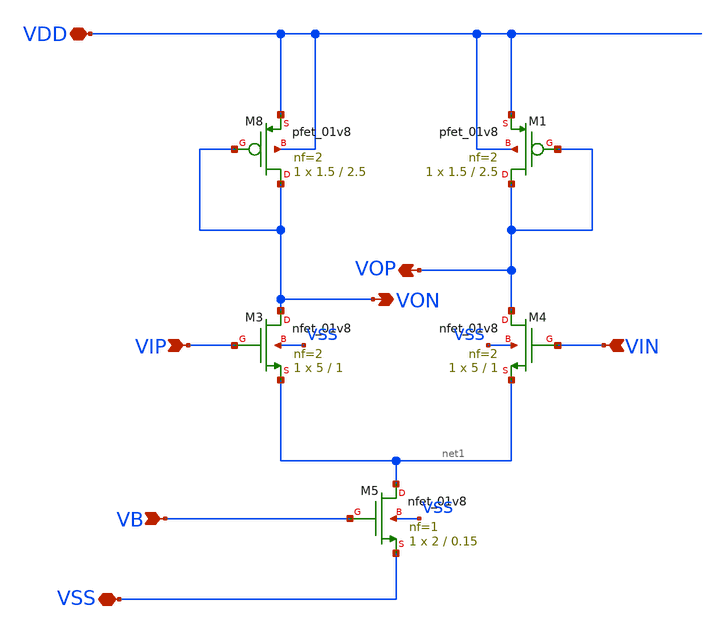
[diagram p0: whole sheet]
** sch_path: xschem/preamp/ota_5t.sch
**.subckt ota_5t VDD VSS VOP VIP VIN VB VON
*.iopin VDD
*.iopin VSS
*.opin VOP
*.ipin VIP
*.ipin VIN
*.ipin VB
*.opin VON
XM3 VON VIP net1 VSS sky130_fd_pr__nfet_01v8 L=1 W=5 nf=2 ad='int((2 + 1)/2) * 5 / 2 * 0.29' as='int((2 + 2)/2) * 5 / 2 * 0.29'
+ pd='2*int((2 + 1)/2) * (5 / 2 + 0.29)' ps='2*int((2 + 2)/2) * (5 / 2 + 0.29)' nrd='0.29 / 5 ' nrs='0.29 / 5 '
+ sa=0 sb=0 sd=0 mult=1 m=1
XM1 VOP VOP VDD VDD sky130_fd_pr__pfet_01v8 L=2.5 W=1.5 nf=2 ad='int((nf+1)/2) * W/nf * 0.29' as='int((nf+2)/2) * W/nf * 0.29'
+ pd='2*int((nf+1)/2) * (W/nf + 0.29)' ps='2*int((nf+2)/2) * (W/nf + 0.29)' nrd='0.29 / W' nrs='0.29 / W'
+ sa=0 sb=0 sd=0 mult=1 m=1
XM4 VOP VIN net1 VSS sky130_fd_pr__nfet_01v8 L=1 W=5 nf=2 ad='int((2 + 1)/2) * 5 / 2 * 0.29' as='int((2 + 2)/2) * 5 / 2 * 0.29'
+ pd='2*int((2 + 1)/2) * (5 / 2 + 0.29)' ps='2*int((2 + 2)/2) * (5 / 2 + 0.29)' nrd='0.29 / 5 ' nrs='0.29 / 5 '
+ sa=0 sb=0 sd=0 mult=1 m=1
XM5 net1 VB VSS VSS sky130_fd_pr__nfet_01v8 L=0.15 W=2 nf=1 ad='int((1 + 1)/2) * 2 / 1 * 0.29' as='int((1 + 2)/2) * 2 / 1 * 0.29'
+ pd='2*int((1 + 1)/2) * (2 / 1 + 0.29)' ps='2*int((1 + 2)/2) * (2 / 1 + 0.29)' nrd='0.29 / 2 ' nrs='0.29 / 2 '
+ sa=0 sb=0 sd=0 mult=1 m=1
XM8 VON VON VDD VDD sky130_fd_pr__pfet_01v8 L=2.5 W=1.5 nf=2 ad='int((nf+1)/2) * W/nf * 0.29' as='int((nf+2)/2) * W/nf * 0.29'
+ pd='2*int((nf+1)/2) * (W/nf + 0.29)' ps='2*int((nf+2)/2) * (W/nf + 0.29)' nrd='0.29 / W' nrs='0.29 / W'
+ sa=0 sb=0 sd=0 mult=1 m=1
**.ends
.end
